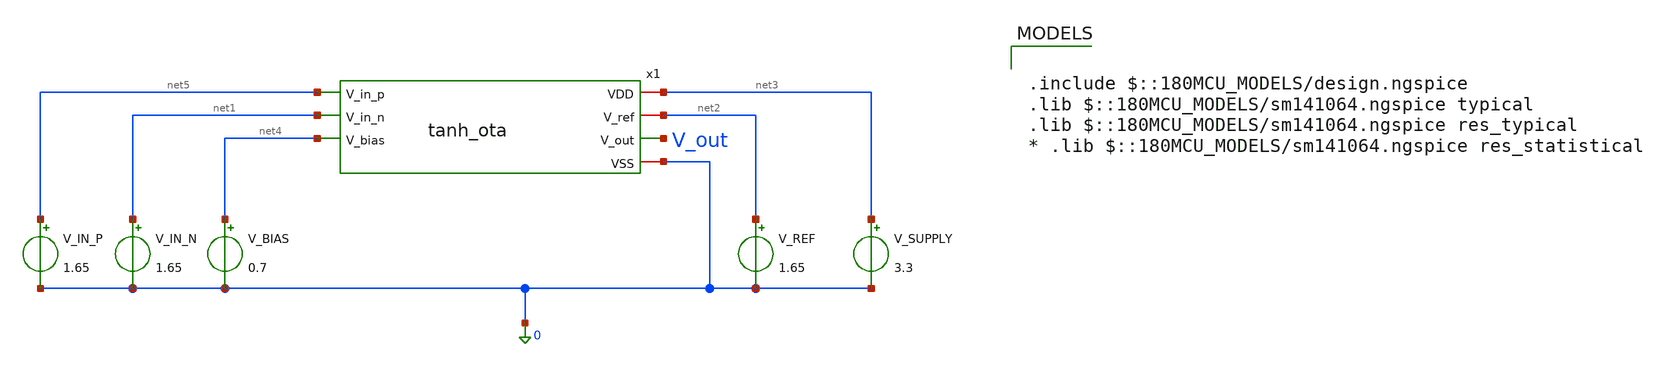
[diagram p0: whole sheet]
** sch_path: schematics/tb_tanh_ota.sch
**.subckt tb_tanh_ota
x1 net3 net2 V_out net5 net1 net4 0 tanh_ota
V_REF net2 0 1.65
V_SUPPLY net3 0 3.3
V_BIAS net4 0 0.7
V_IN_N net1 0 1.65
V_IN_P net5 0 1.65
**** begin user architecture code

.include $::180MCU_MODELS/design.ngspice
.lib $::180MCU_MODELS/sm141064.ngspice typical
.lib $::180MCU_MODELS/sm141064.ngspice res_typical
* .lib $::180MCU_MODELS/sm141064.ngspice res_statistical



.control
  dc V_IN_P 1.4 1.9 0.002
  let V_out = v(V_out)
  plot V_out title "tanh OTA: Saturating Transfer Characteristic"
  wrdata /foss/designs/analog-perceptron-gf180mcu/plots/tanh_ota_sweep.txt V_out
.endc


**** end user architecture code
**.ends

* expanding   symbol:  analog-perceptron-gf180mcu/schematics/tanh_ota.sym # of pins=7
** sym_path: schematics/tanh_ota.sym
** sch_path: schematics/tanh_ota.sch
.subckt tanh_ota VDD V_ref V_out V_in_p V_in_n V_bias VSS
*.iopin VDD
*.iopin VSS
*.ipin V_in_p
*.ipin V_in_n
*.ipin V_bias
*.opin V_out
*.iopin V_ref
XM1 net2 V_in_p net1 VSS nfet_03v3 L=0.5u W=10u nf=1 ad='int((nf+1)/2) * W/nf * 0.18u' as='int((nf+2)/2) * W/nf * 0.18u'
+ pd='2*int((nf+1)/2) * (W/nf + 0.18u)' ps='2*int((nf+2)/2) * (W/nf + 0.18u)' nrd='0.18u / W' nrs='0.18u / W'
+ sa=0 sb=0 sd=0 m=1
XM2 V_out V_in_n net1 VSS nfet_03v3 L=0.5u W=10u nf=1 ad='int((nf+1)/2) * W/nf * 0.18u' as='int((nf+2)/2) * W/nf * 0.18u'
+ pd='2*int((nf+1)/2) * (W/nf + 0.18u)' ps='2*int((nf+2)/2) * (W/nf + 0.18u)' nrd='0.18u / W' nrs='0.18u / W'
+ sa=0 sb=0 sd=0 m=1
XM3 net1 V_bias VSS VSS nfet_03v3 L=0.5u W=10u nf=1 ad='int((nf+1)/2) * W/nf * 0.18u' as='int((nf+2)/2) * W/nf * 0.18u'
+ pd='2*int((nf+1)/2) * (W/nf + 0.18u)' ps='2*int((nf+2)/2) * (W/nf + 0.18u)' nrd='0.18u / W' nrs='0.18u / W'
+ sa=0 sb=0 sd=0 m=1
XM4 net2 net2 VDD VDD pfet_03v3 L=0.5u W=20u nf=1 ad='int((nf+1)/2) * W/nf * 0.18u' as='int((nf+2)/2) * W/nf * 0.18u'
+ pd='2*int((nf+1)/2) * (W/nf + 0.18u)' ps='2*int((nf+2)/2) * (W/nf + 0.18u)' nrd='0.18u / W' nrs='0.18u / W'
+ sa=0 sb=0 sd=0 m=1
XM5 V_out net2 VDD VDD pfet_03v3 L=0.5u W=20u nf=1 ad='int((nf+1)/2) * W/nf * 0.18u' as='int((nf+2)/2) * W/nf * 0.18u'
+ pd='2*int((nf+1)/2) * (W/nf + 0.18u)' ps='2*int((nf+2)/2) * (W/nf + 0.18u)' nrd='0.18u / W' nrs='0.18u / W'
+ sa=0 sb=0 sd=0 m=1
XR1 net3 V_ref VSS ppolyf_u_1k r_width=3e-6 r_length=12.4e-6 m=1
XR2 net4 net3 VSS ppolyf_u_1k r_width=3e-6 r_length=12.4e-6 m=1
XR3 net5 net4 VSS ppolyf_u_1k r_width=3e-6 r_length=12.4e-6 m=1
XR4 net6 net5 VSS ppolyf_u_1k r_width=3e-6 r_length=12.4e-6 m=1
XR5 net7 net6 VSS ppolyf_u_1k r_width=3e-6 r_length=12.4e-6 m=1
XR6 V_out net7 VSS ppolyf_u_1k r_width=3e-6 r_length=12.4e-6 m=1
.ends

.end
